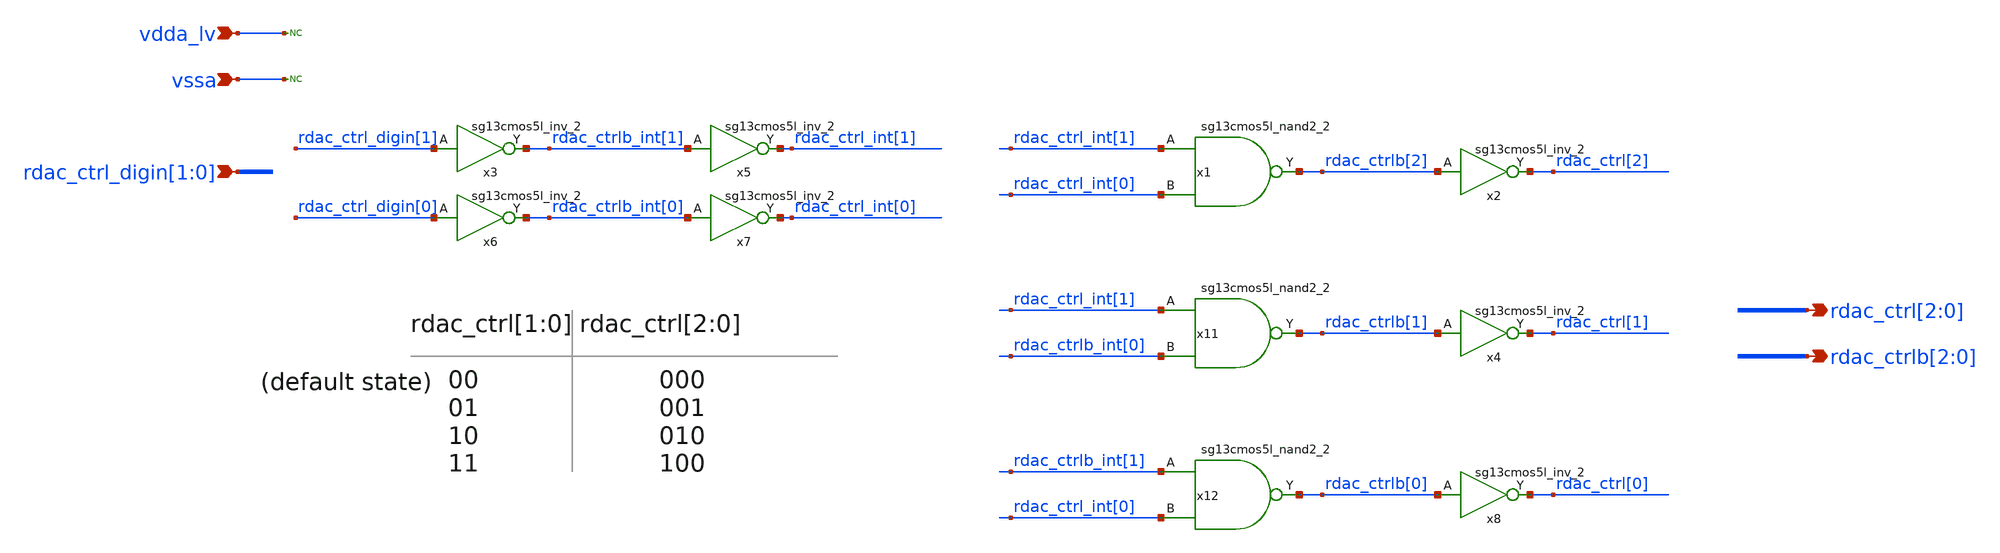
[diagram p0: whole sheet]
** sch_path: Schematics_Layout/sunrise_rdac_ctrl/sunrise_rdac_ctrl.sch
**.subckt sunrise_rdac_ctrl rdac_ctrl_digin[1],rdac_ctrl_digin[0]
*+ rdac_ctrl[2],rdac_ctrl[1],rdac_ctrl[0] vdda_lv vssa rdac_ctrlb[2],rdac_ctrlb[1],rdac_ctrlb[0]
*.ipin rdac_ctrl_digin[1],rdac_ctrl_digin[0]
*.opin rdac_ctrl[2],rdac_ctrl[1],rdac_ctrl[0]
*.ipin vdda_lv
*.ipin vssa
*.opin rdac_ctrlb[2],rdac_ctrlb[1],rdac_ctrlb[0]
* noconn vdda_lv
* noconn vssa
x3 rdac_ctrlb_int[1] rdac_ctrl_digin[1] vdda_lv vssa sg13cmos5l_inv_2
x5 rdac_ctrl_int[1] rdac_ctrlb_int[1] vdda_lv vssa sg13cmos5l_inv_2
x6 rdac_ctrlb_int[0] rdac_ctrl_digin[0] vdda_lv vssa sg13cmos5l_inv_2
x7 rdac_ctrl_int[0] rdac_ctrlb_int[0] vdda_lv vssa sg13cmos5l_inv_2
x1 rdac_ctrlb[2] rdac_ctrl_int[1] rdac_ctrl_int[0] vdda_lv vssa sg13cmos5l_nand2_2
x2 rdac_ctrl[2] rdac_ctrlb[2] vdda_lv vssa sg13cmos5l_inv_2
x4 rdac_ctrl[1] rdac_ctrlb[1] vdda_lv vssa sg13cmos5l_inv_2
x8 rdac_ctrl[0] rdac_ctrlb[0] vdda_lv vssa sg13cmos5l_inv_2
x11 rdac_ctrlb[1] rdac_ctrl_int[1] rdac_ctrlb_int[0] vdda_lv vssa sg13cmos5l_nand2_2
x12 rdac_ctrlb[0] rdac_ctrlb_int[1] rdac_ctrl_int[0] vdda_lv vssa sg13cmos5l_nand2_2
**.ends
.end
